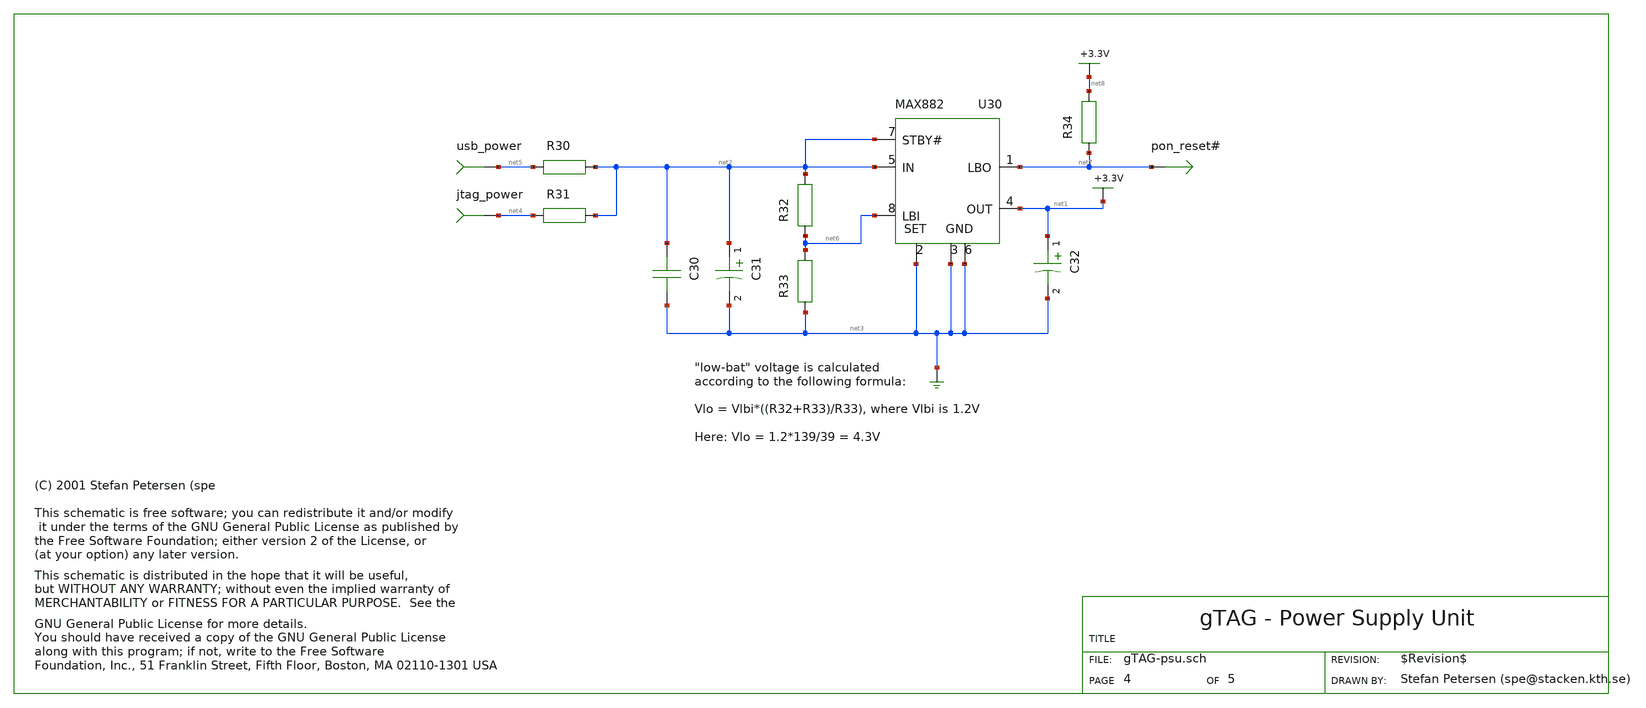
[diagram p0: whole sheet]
** sch_path: xschem_library/gschem_import/gTAG-psu.sch
* copyleft.sym
**.subckt gTAG-psu
usb_power net5
jtag_power net4
U30 net2 net6 net2 net1 net3 net3 net3 net7
C32 net1 net3 2.2u
C31 net2 net3 2.2u
R30 net2 net5 0
R31 net2 net4 0
C30 net2 net3 100n
R33 net6 net3 39k
R32 net2 net6 100k
R34 net8 net7 10k
pon_reset# net7
**.ends
.end
